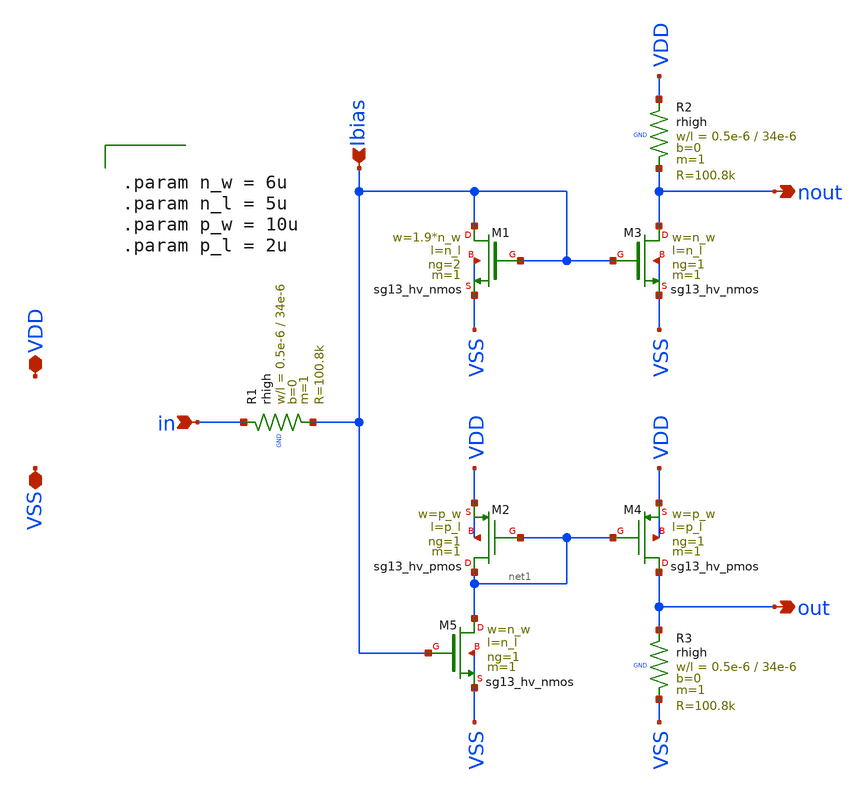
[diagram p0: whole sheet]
** sch_path: macros/heichips26_vcr/macros/switched_capacitor/schematic/xschem/voltage_mirror.sch
**.subckt voltage_mirror VDD VSS in out nout Ibias
*.iopin VDD
*.iopin VSS
*.ipin in
*.opin out
*.opin nout
*.ipin Ibias
XM1 Ibias Ibias VSS VSS sg13_hv_nmos w=1.9*n_w l=n_l ng=2 m=1 mm_ok=1
XR1 in Ibias GND rhigh w=0.5e-6 l=34e-6 m=1 b=0 mm_ok=1
XM2 net1 net1 VDD VDD sg13_hv_pmos w=p_w l=p_l ng=1 m=1 mm_ok=1
XM3 nout Ibias VSS VSS sg13_hv_nmos w=n_w l=n_l ng=1 m=1 mm_ok=1
XM4 out net1 VDD VDD sg13_hv_pmos w=p_w l=p_l ng=1 m=1 mm_ok=1
XM5 net1 Ibias VSS VSS sg13_hv_nmos w=n_w l=n_l ng=1 m=1 mm_ok=1
XR2 VDD nout GND rhigh w=0.5e-6 l=34e-6 m=1 b=0 mm_ok=1
XR3 out VSS GND rhigh w=0.5e-6 l=34e-6 m=1 b=0 mm_ok=1
**** begin user architecture code


.param n_w = 6u
.param n_l = 5u
.param p_w = 10u
.param p_l = 2u


**** end user architecture code
**.ends
.end
